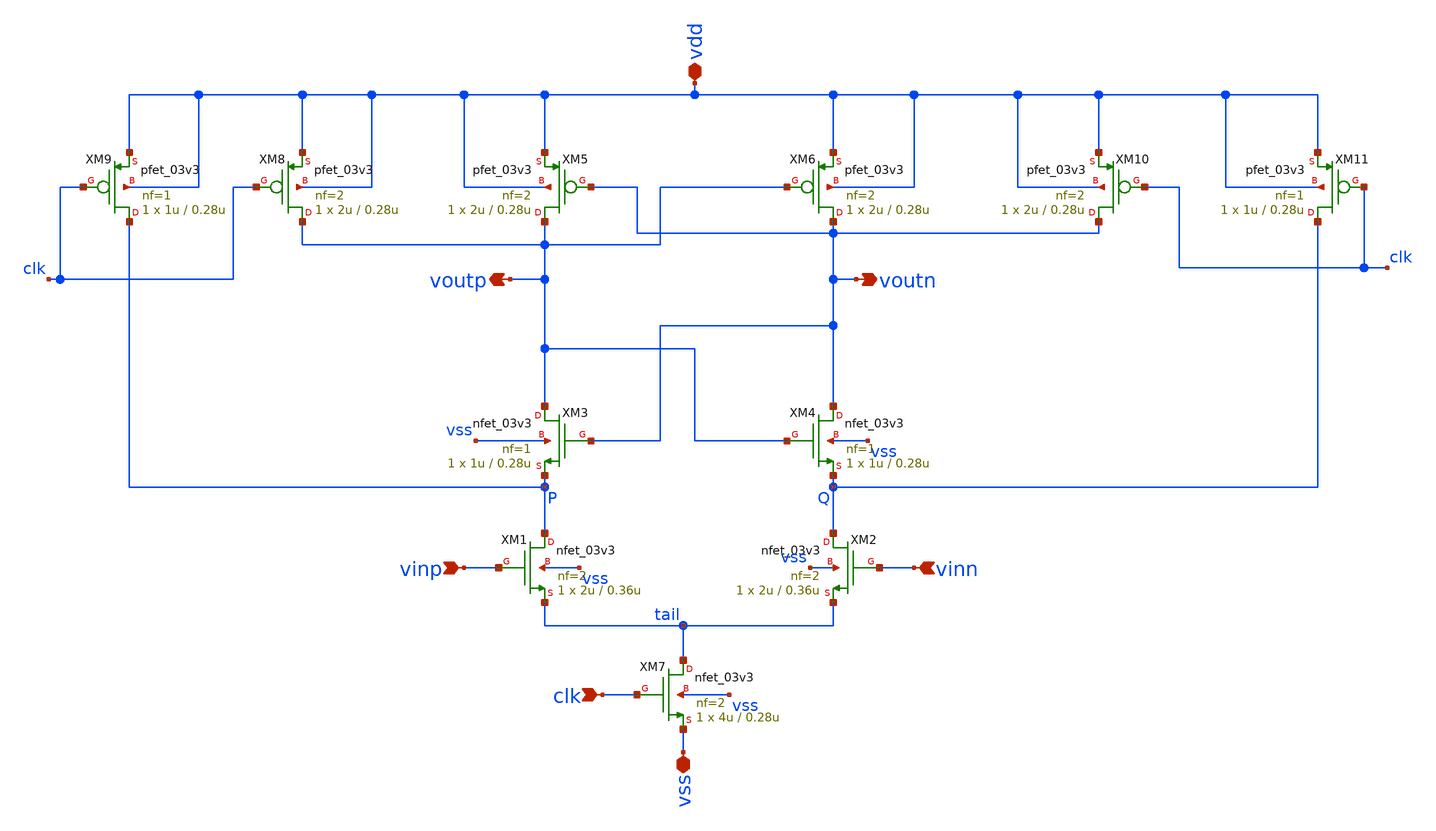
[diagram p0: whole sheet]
** sch_path: designs/libs/core_analog/comp/comp.sch
**.subckt comp vss vdd vinp vinn clk voutn voutp
*.iopin vss
*.iopin vdd
*.ipin vinp
*.ipin vinn
*.ipin clk
*.opin voutn
*.opin voutp
XM1 P vinp tail vss nfet_03v3 L=0.36u W=2u nf=2 ad='int((nf+1)/2) * W/nf * 0.18u' as='int((nf+2)/2) * W/nf * 0.18u'
+ pd='2*int((nf+1)/2) * (W/nf + 0.18u)' ps='2*int((nf+2)/2) * (W/nf + 0.18u)' nrd='0.18u / W' nrs='0.18u / W'
+ sa=0 sb=0 sd=0 m=1
XM2 Q vinn tail vss nfet_03v3 L=0.36u W=2u nf=2 ad='int((nf+1)/2) * W/nf * 0.18u' as='int((nf+2)/2) * W/nf * 0.18u'
+ pd='2*int((nf+1)/2) * (W/nf + 0.18u)' ps='2*int((nf+2)/2) * (W/nf + 0.18u)' nrd='0.18u / W' nrs='0.18u / W'
+ sa=0 sb=0 sd=0 m=1
XM7 tail clk vss vss nfet_03v3 L=0.28u W=4u nf=2 ad='int((nf+1)/2) * W/nf * 0.18u' as='int((nf+2)/2) * W/nf * 0.18u'
+ pd='2*int((nf+1)/2) * (W/nf + 0.18u)' ps='2*int((nf+2)/2) * (W/nf + 0.18u)' nrd='0.18u / W' nrs='0.18u / W'
+ sa=0 sb=0 sd=0 m=1
XM3 voutp voutn P vss nfet_03v3 L=0.28u W=1u nf=1 ad='int((nf+1)/2) * W/nf * 0.18u' as='int((nf+2)/2) * W/nf * 0.18u'
+ pd='2*int((nf+1)/2) * (W/nf + 0.18u)' ps='2*int((nf+2)/2) * (W/nf + 0.18u)' nrd='0.18u / W' nrs='0.18u / W'
+ sa=0 sb=0 sd=0 m=1
XM4 voutn voutp Q vss nfet_03v3 L=0.28u W=1u nf=1 ad='int((nf+1)/2) * W/nf * 0.18u' as='int((nf+2)/2) * W/nf * 0.18u'
+ pd='2*int((nf+1)/2) * (W/nf + 0.18u)' ps='2*int((nf+2)/2) * (W/nf + 0.18u)' nrd='0.18u / W' nrs='0.18u / W'
+ sa=0 sb=0 sd=0 m=1
XM6 voutn voutp vdd vdd pfet_03v3 L=0.28u W=2u nf=2 ad='int((nf+1)/2) * W/nf * 0.18u' as='int((nf+2)/2) * W/nf * 0.18u'
+ pd='2*int((nf+1)/2) * (W/nf + 0.18u)' ps='2*int((nf+2)/2) * (W/nf + 0.18u)' nrd='0.18u / W' nrs='0.18u / W'
+ sa=0 sb=0 sd=0 m=1
XM5 voutp voutn vdd vdd pfet_03v3 L=0.28u W=2u nf=2 ad='int((nf+1)/2) * W/nf * 0.18u' as='int((nf+2)/2) * W/nf * 0.18u'
+ pd='2*int((nf+1)/2) * (W/nf + 0.18u)' ps='2*int((nf+2)/2) * (W/nf + 0.18u)' nrd='0.18u / W' nrs='0.18u / W'
+ sa=0 sb=0 sd=0 m=1
XM10 voutn clk vdd vdd pfet_03v3 L=0.28u W=2u nf=2 ad='int((nf+1)/2) * W/nf * 0.18u' as='int((nf+2)/2) * W/nf * 0.18u'
+ pd='2*int((nf+1)/2) * (W/nf + 0.18u)' ps='2*int((nf+2)/2) * (W/nf + 0.18u)' nrd='0.18u / W' nrs='0.18u / W'
+ sa=0 sb=0 sd=0 m=1
XM11 Q clk vdd vdd pfet_03v3 L=0.28u W=1u nf=1 ad='int((nf+1)/2) * W/nf * 0.18u' as='int((nf+2)/2) * W/nf * 0.18u'
+ pd='2*int((nf+1)/2) * (W/nf + 0.18u)' ps='2*int((nf+2)/2) * (W/nf + 0.18u)' nrd='0.18u / W' nrs='0.18u / W'
+ sa=0 sb=0 sd=0 m=1
XM8 voutp clk vdd vdd pfet_03v3 L=0.28u W=2u nf=2 ad='int((nf+1)/2) * W/nf * 0.18u' as='int((nf+2)/2) * W/nf * 0.18u'
+ pd='2*int((nf+1)/2) * (W/nf + 0.18u)' ps='2*int((nf+2)/2) * (W/nf + 0.18u)' nrd='0.18u / W' nrs='0.18u / W'
+ sa=0 sb=0 sd=0 m=1
XM9 P clk vdd vdd pfet_03v3 L=0.28u W=1u nf=1 ad='int((nf+1)/2) * W/nf * 0.18u' as='int((nf+2)/2) * W/nf * 0.18u'
+ pd='2*int((nf+1)/2) * (W/nf + 0.18u)' ps='2*int((nf+2)/2) * (W/nf + 0.18u)' nrd='0.18u / W' nrs='0.18u / W'
+ sa=0 sb=0 sd=0 m=1
**.ends
.end
